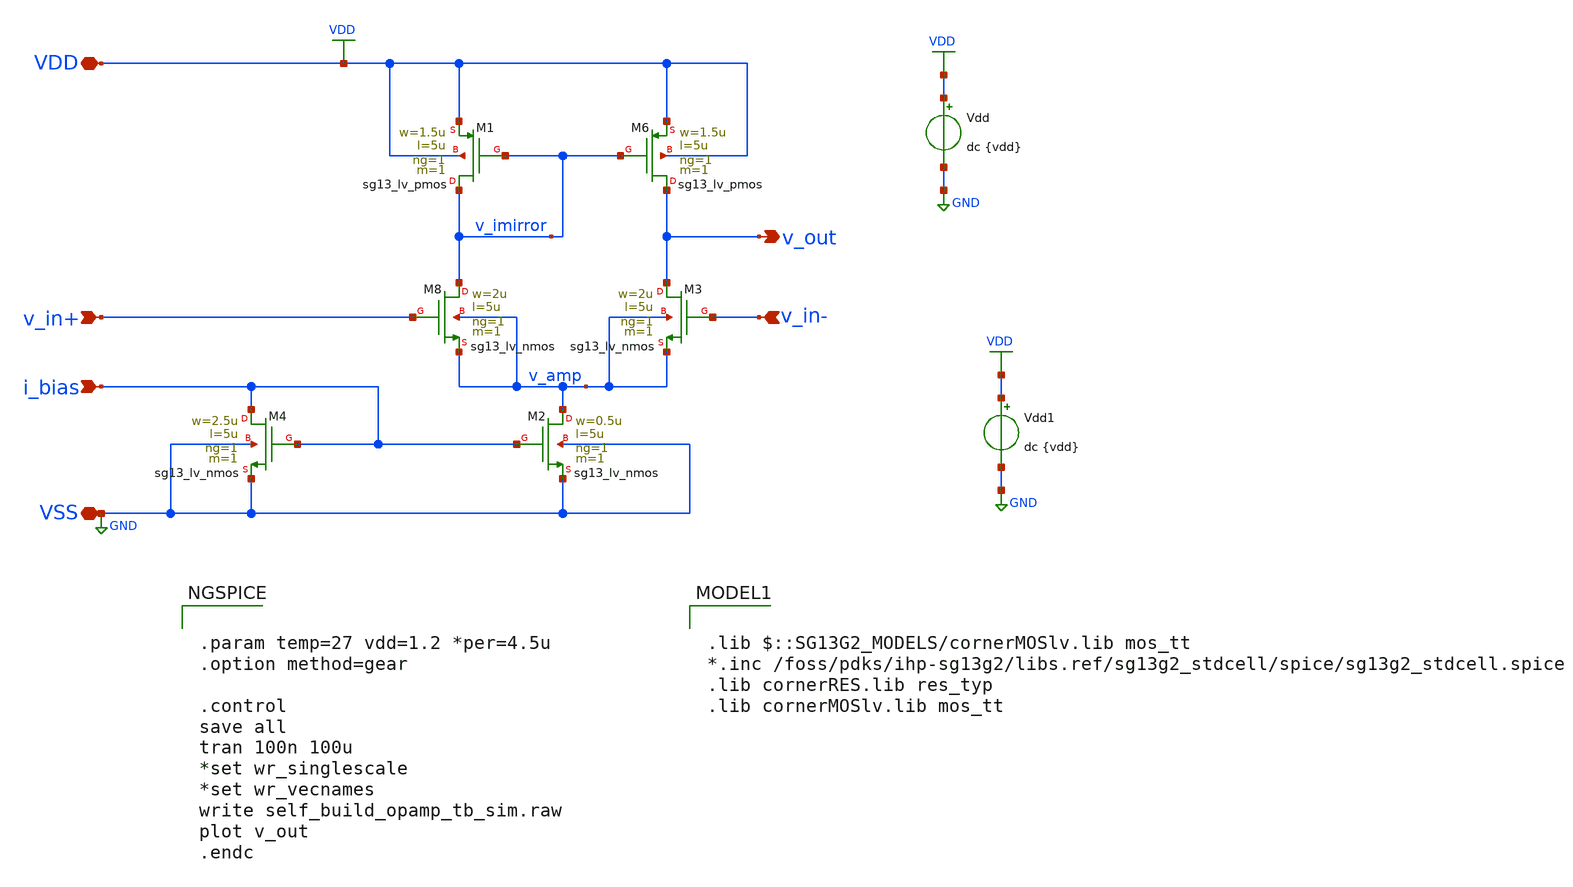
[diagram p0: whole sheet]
** sch_path: 3_Real_Cir/20_Real_Cir/self_build_opamp.sch
**.subckt self_build_opamp v_in+ v_in- v_out VDD VSS i_bias
*.ipin v_in+
*.ipin v_in-
*.opin v_out
*.iopin VDD
*.iopin VSS
*.ipin i_bias
Vdd VDD GND dc {vdd}
Vdd1 VDD GND dc {vdd}
XM8 v_imirror v_in+ v_amp v_amp sg13_lv_nmos w=2u l=5u ng=1 m=1 mm_ok=1
XM3 v_out v_in- v_amp v_amp sg13_lv_nmos w=2u l=5u ng=1 m=1 mm_ok=1
XM2 v_amp i_bias VSS VSS sg13_lv_nmos w=0.5u l=5u ng=1 m=1 mm_ok=1
XM4 i_bias i_bias VSS VSS sg13_lv_nmos w=2.5u l=5u ng=1 m=1 mm_ok=1
XM6 v_out v_imirror VDD VDD sg13_lv_pmos w=1.5u l=5u ng=1 m=1 mm_ok=1
XM1 v_imirror v_imirror VDD VDD sg13_lv_pmos w=1.5u l=5u ng=1 m=1 mm_ok=1
**** begin user architecture code

.lib $::SG13G2_MODELS/cornerMOSlv.lib mos_tt
*.inc /foss/pdks/ihp-sg13g2/libs.ref/sg13g2_stdcell/spice/sg13g2_stdcell.spice
.lib cornerRES.lib res_typ
.lib cornerMOSlv.lib mos_tt



.param temp=27 vdd=1.2 *per=4.5u
.option method=gear

.control
save all
tran 100n 100u
*set wr_singlescale
*set wr_vecnames
write self_build_opamp_tb_sim.raw
plot v_out
.endc


**** end user architecture code
**.ends
.GLOBAL GND
.GLOBAL VDD
.end
